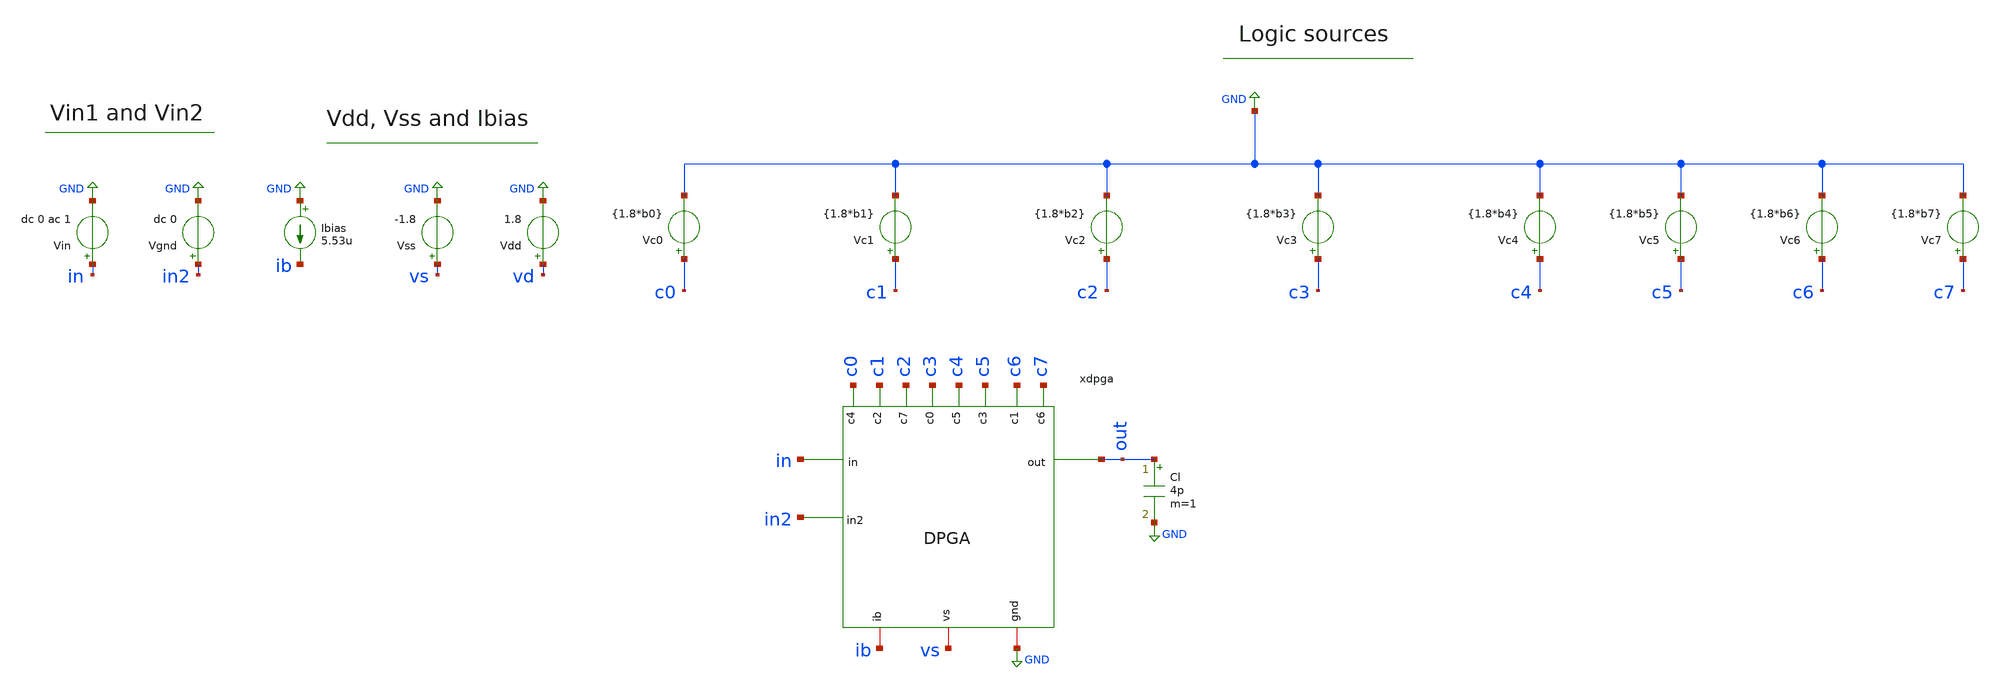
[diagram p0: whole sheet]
** sch_path: xschem/dpga-tb.sch
**.subckt dpga-tb
Vdd vd GND 1.8
Vc0 c0 GND {1.8*b0}
Vc1 c1 GND {1.8*b1}
Vc2 c2 GND {1.8*b2}
Vc3 c3 GND {1.8*b3}
Vc4 c4 GND {1.8*b4}
Vc5 c5 GND {1.8*b5}
Vc6 c6 GND {1.8*b6}
Vc7 c7 GND {1.8*b7}
Vss vs GND -1.8
Ibias GND ib 5.53u
Vgnd in2 GND dc 0
Vin in GND dc 0 ac 1
Cl out GND 4p m=1
x1 GND c7 c6 c5 c4 c3 c2 c1 c0 out in in2 vs ib dpga
**** begin user architecture code

.end
.lib /edatools/pdks/sky130A/libs.tech/ngspice/sky130.lib.spice tt
*.include /home/hugodg/sky130_skel/dpga-ieee-sscs-contest-main/minimal_libs/sky130_libs/sky130_lib.spice


.ac dec 2000 1 5Meg

*.tran 0.01m 10m
.end

.control
set color0=white
set color1=black
destroy all
run
let gain=abs(out/in)
plot gain
.endc


.param b7=1 b6=1 b5=1 b4=1 b3=1 b2=1 b1=1 b0=1

**** end user architecture code
**.ends
.GLOBAL GND
.end
